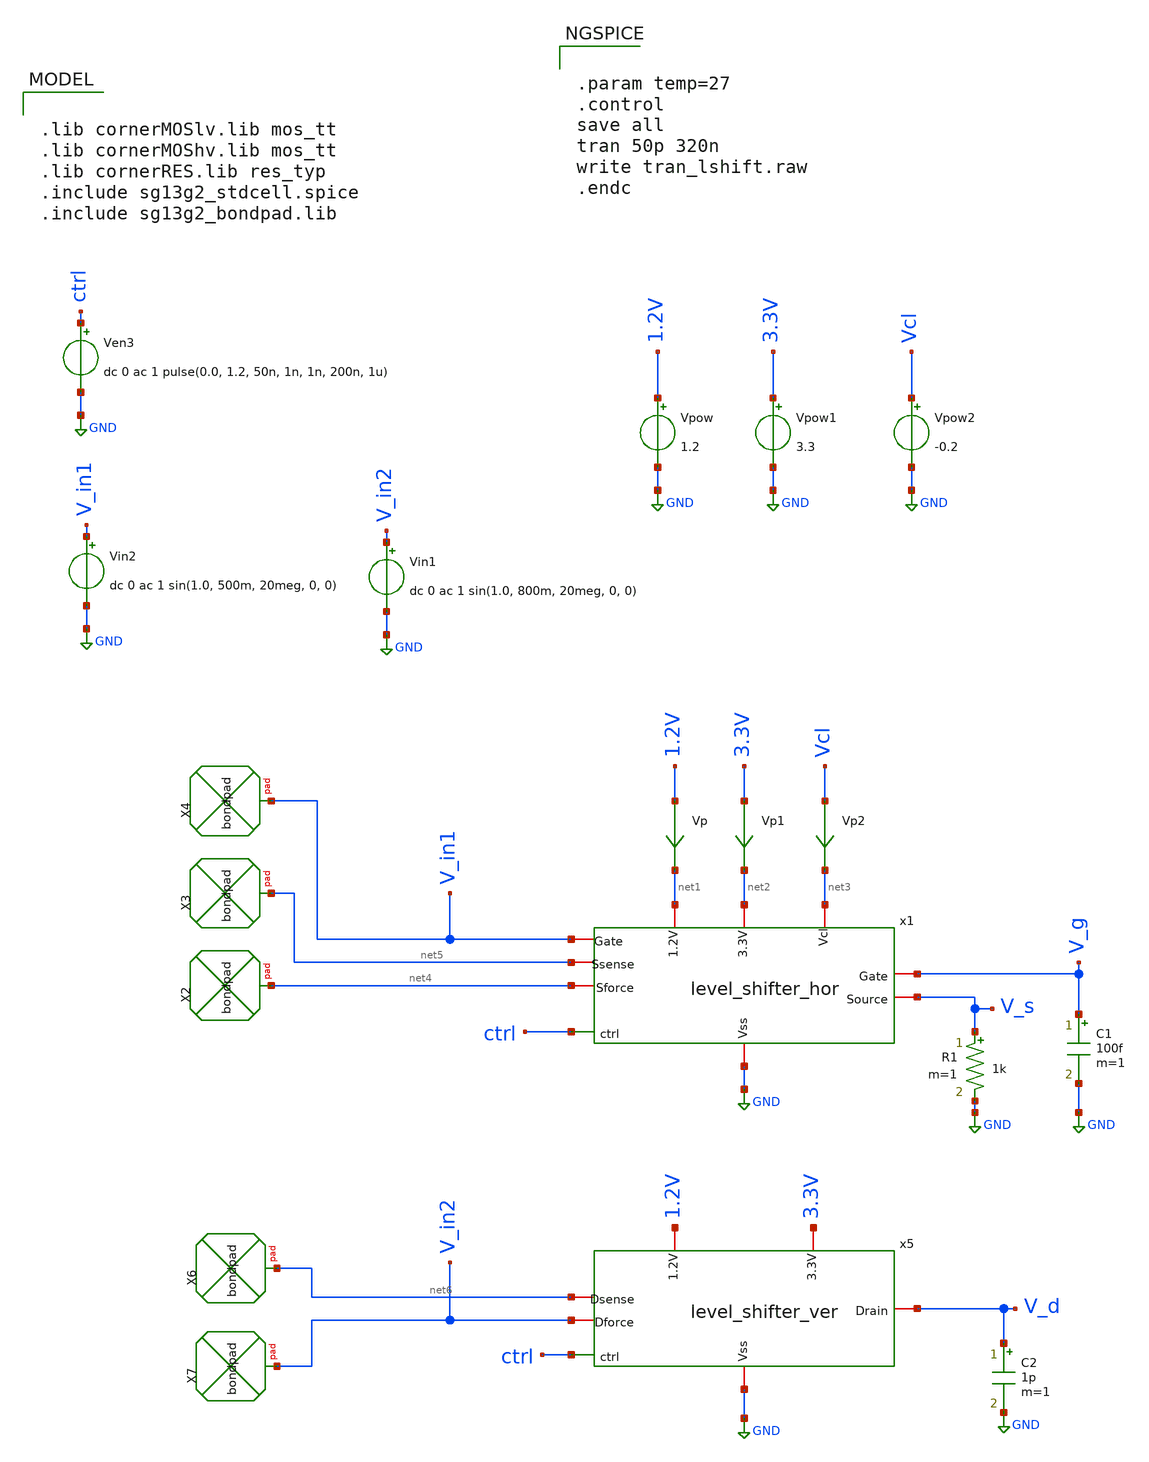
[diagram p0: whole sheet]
** sch_path: design_data/xschem/level_shifter_tran_tb.sch
* Copyright 2023 IHP PDK Authors
* design_data/xschem/level_shifter_hor.sch:
* Copyright 2025 IHP PDK Authors
**.subckt level_shifter_tran_tb
Vpow 1.2V GND 1.2
Vp 1.2V net1 0
.save i(vp)
C1 V_g GND 100f m=1
Ven3 ctrl GND dc 0 ac 1 pulse(0.0, 1.2, 50n, 1n, 1n, 200n, 1u)
Vin2 V_in1 GND dc 0 ac 1 sin(1.0, 500m, 20meg, 0, 0)
Vpow1 3.3V GND 3.3
Vp1 3.3V net2 0
.save i(vp1)
Vp2 Vcl net3 0
.save i(vp2)
Vpow2 Vcl GND -0.2
R1 V_s GND 1k m=1
XX2 net4 bondpad size=80u shape=0 padtype=0
XX3 net5 bondpad size=80u shape=0 padtype=0
XX4 V_in1 bondpad size=80u shape=0 padtype=0
x1 net1 net5 net3 ctrl V_s GND net2 V_g V_in1 net4 level_shifter_hor
x5 1.2V net6 ctrl V_d GND 3.3V V_in2 level_shifter_ver
XX6 net6 bondpad size=80u shape=0 padtype=0
XX7 V_in2 bondpad size=80u shape=0 padtype=0
Vin1 V_in2 GND dc 0 ac 1 sin(1.0, 800m, 20meg, 0, 0)
C2 V_d GND 1p m=1
**** begin user architecture code

.lib cornerMOSlv.lib mos_tt
.lib cornerMOShv.lib mos_tt
.lib cornerRES.lib res_typ
.include sg13g2_stdcell.spice
.include sg13g2_bondpad.lib



.param temp=27
.control
save all
tran 50p 320n
write tran_lshift.raw
.endc


**** end user architecture code
**.ends

* expanding   symbol:  level_shifter_hor.sym # of pins=10
** sym_path: design_data/xschem/level_shifter_hor.sym
** sch_path: design_data/xschem/level_shifter_hor.sch
.subckt level_shifter_hor 1.2V Ssense Vcl ctrl Source Vss 3.3V Gate G2 Sforce
*.iopin Gate
*.iopin Vss
*.iopin G2
*.iopin 3.3V
*.ipin ctrl
*.iopin 1.2V
*.iopin Vcl
*.iopin Ssense
*.iopin Source
*.iopin Sforce
XM2 net1 net3 3.3V 3.3V sg13_hv_pmos w=0.3u l=0.4u ng=1 m=1 mm_ok=1
XM3 net2 ctrl Vss Vss sg13_lv_nmos w=0.15u l=0.13u ng=1 m=1 mm_ok=1
XM5 net2 ctrl 1.2V 1.2V sg13_lv_pmos w=0.3u l=0.13u ng=1 m=1 mm_ok=1
XM1 net3 net1 3.3V 3.3V sg13_hv_pmos w=0.3u l=0.4u ng=1 m=1 mm_ok=1
XM4 Gate net3 G2 3.3V sg13_hv_pmos w=1.3u l=0.4u ng=1 m=1 mm_ok=1
XM8 G2 net1 Gate Vss sg13_hv_nmos w=1.3u l=0.45u ng=1 m=1 mm_ok=1
XM6 net3 net2 Vss Vss sg13_hv_nmos w=1.0u l=0.45u ng=1 m=1 mm_ok=1
XM7 net1 ctrl Vss Vss sg13_hv_nmos w=1.0u l=0.45u ng=1 m=1 mm_ok=1
XM9 Vcl net3 Gate Vss sg13_hv_nmos w=1.3u l=0.45u ng=1 m=1 mm_ok=1
XM12 Source net3 Sforce 3.3V sg13_hv_pmos w=16u l=0.4u ng=5 m=1 mm_ok=1
XM13 Sforce net1 Source Vss sg13_hv_nmos w=8u l=0.45u ng=5 m=1 mm_ok=1
R1 Ssense Source 0.1 m=1
.ends


* expanding   symbol:  level_shifter_ver.sym # of pins=7
** sym_path: design_data/xschem/level_shifter_ver.sym
** sch_path: design_data/xschem/level_shifter_ver.sch
.subckt level_shifter_ver 1.2V Dsense ctrl Drain Vss 3.3V Dforce
*.iopin Vss
*.iopin 3.3V
*.ipin ctrl
*.iopin 1.2V
*.iopin Dsense
*.iopin Drain
*.iopin Dforce
XM2 net1 net3 3.3V 3.3V sg13_hv_pmos w=0.3u l=0.4u ng=1 m=1 mm_ok=1
XM3 net2 ctrl Vss Vss sg13_lv_nmos w=0.15u l=0.13u ng=1 m=1 mm_ok=1
XM5 net2 ctrl 1.2V 1.2V sg13_lv_pmos w=0.30u l=0.13u ng=1 m=1 mm_ok=1
XM1 net3 net1 3.3V 3.3V sg13_hv_pmos w=0.3u l=0.4u ng=1 m=1 mm_ok=1
XM6 net3 net2 Vss Vss sg13_hv_nmos w=1.0u l=0.45u ng=1 m=1 mm_ok=1
XM7 net1 ctrl Vss Vss sg13_hv_nmos w=1.0u l=0.45u ng=1 m=1 mm_ok=1
XM12 Drain net3 Dforce 3.3V sg13_hv_pmos w=16u l=0.4u ng=5 m=1 mm_ok=1
XM13 Dforce net1 Drain Vss sg13_hv_nmos w=8u l=0.45u ng=5 m=1 mm_ok=1
R1 Dsense Drain 0.1 m=1
.ends

.GLOBAL GND
.end
